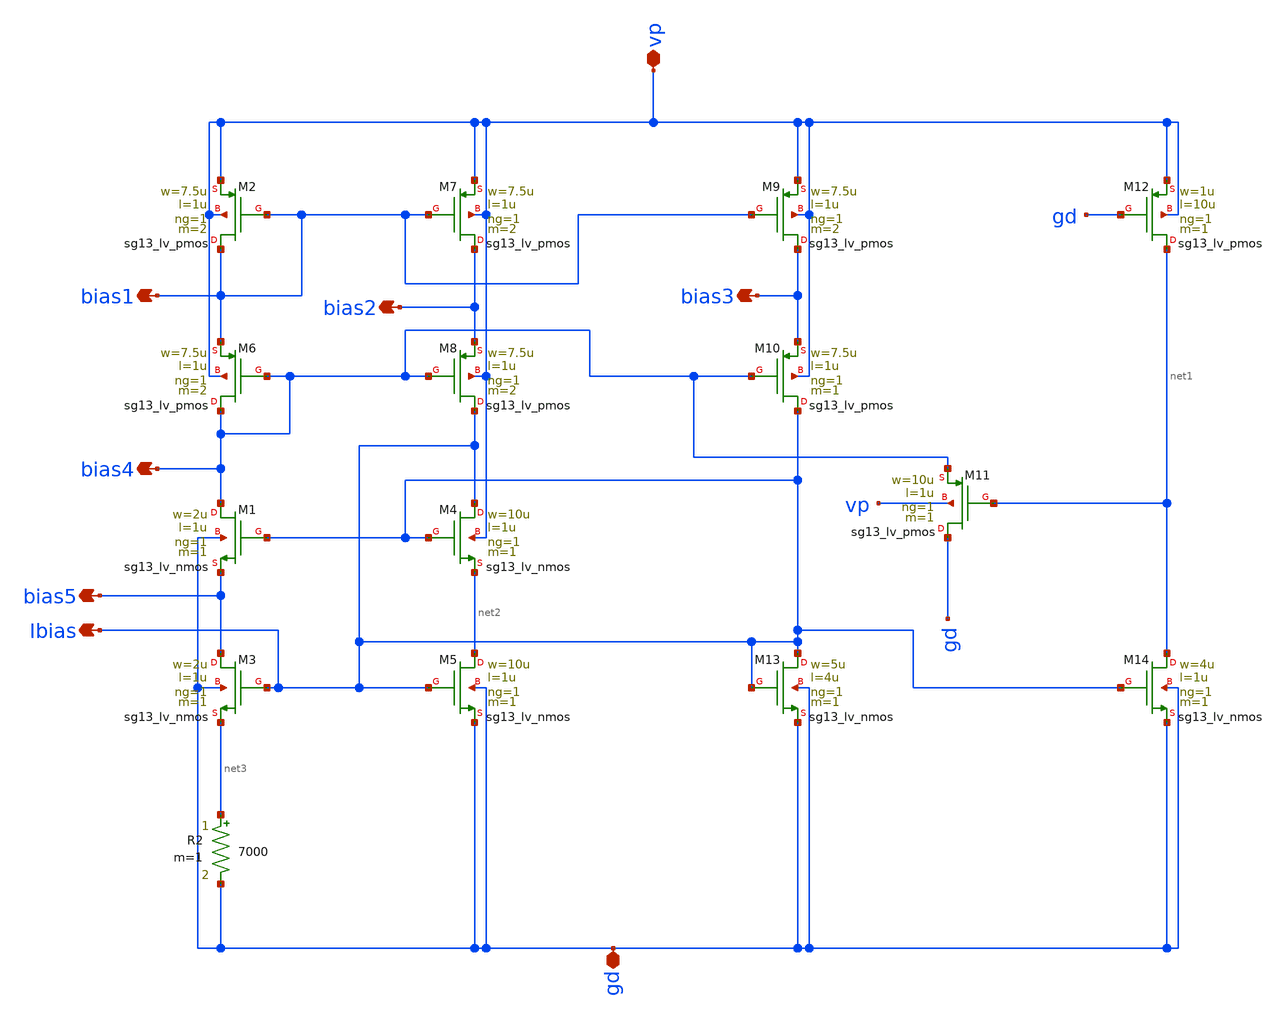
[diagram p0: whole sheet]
** sch_path: schematics/charge_pump/vbias/vbias_v2.sch
**.subckt vbias_v2 vp bias1 bias2 bias4 Ibias bias5 gd bias3
*.iopin vp
*.opin bias1
*.opin bias2
*.opin bias4
*.opin Ibias
*.opin bias5
*.iopin gd
*.opin bias3
XM1 bias4 Ibias bias5 gd sg13_lv_nmos w=2u l=1u ng=1 m=1 mm_ok=1
XM2 bias1 bias1 vp vp sg13_lv_pmos w=7.5u l=1u ng=1 m=2 mm_ok=1
XM4 Ibias Ibias net2 vp sg13_lv_nmos w=10u l=1u ng=1 m=1 mm_ok=1
XM5 net2 Ibias gd gd sg13_lv_nmos w=10u l=1u ng=1 m=1 mm_ok=1
XM6 bias4 bias4 bias1 vp sg13_lv_pmos w=7.5u l=1u ng=1 m=2 mm_ok=1
XM7 bias2 bias1 vp vp sg13_lv_pmos w=7.5u l=1u ng=1 m=2 mm_ok=1
XM8 Ibias bias4 bias2 vp sg13_lv_pmos w=7.5u l=1u ng=1 m=2 mm_ok=1
R2 net3 gd 7000 m=1
XM11 gd net1 bias4 vp sg13_lv_pmos w=10u l=1u ng=1 m=1 mm_ok=1
XM12 net1 gd vp vp sg13_lv_pmos w=1u l=10u ng=1 m=1 mm_ok=1
XM3 bias5 Ibias net3 gd sg13_lv_nmos w=2u l=1u ng=1 m=1 mm_ok=1
XM14 net1 Ibias gd gd sg13_lv_nmos w=4u l=1u ng=1 m=1 mm_ok=1
XM13 Ibias Ibias gd gd sg13_lv_nmos w=5u l=4u ng=1 m=1 mm_ok=1
XM10 Ibias bias4 bias3 vp sg13_lv_pmos w=7.5u l=1u ng=1 m=1 mm_ok=1
XM9 bias3 bias1 vp vp sg13_lv_pmos w=7.5u l=1u ng=1 m=2 mm_ok=1
**.ends
.end
